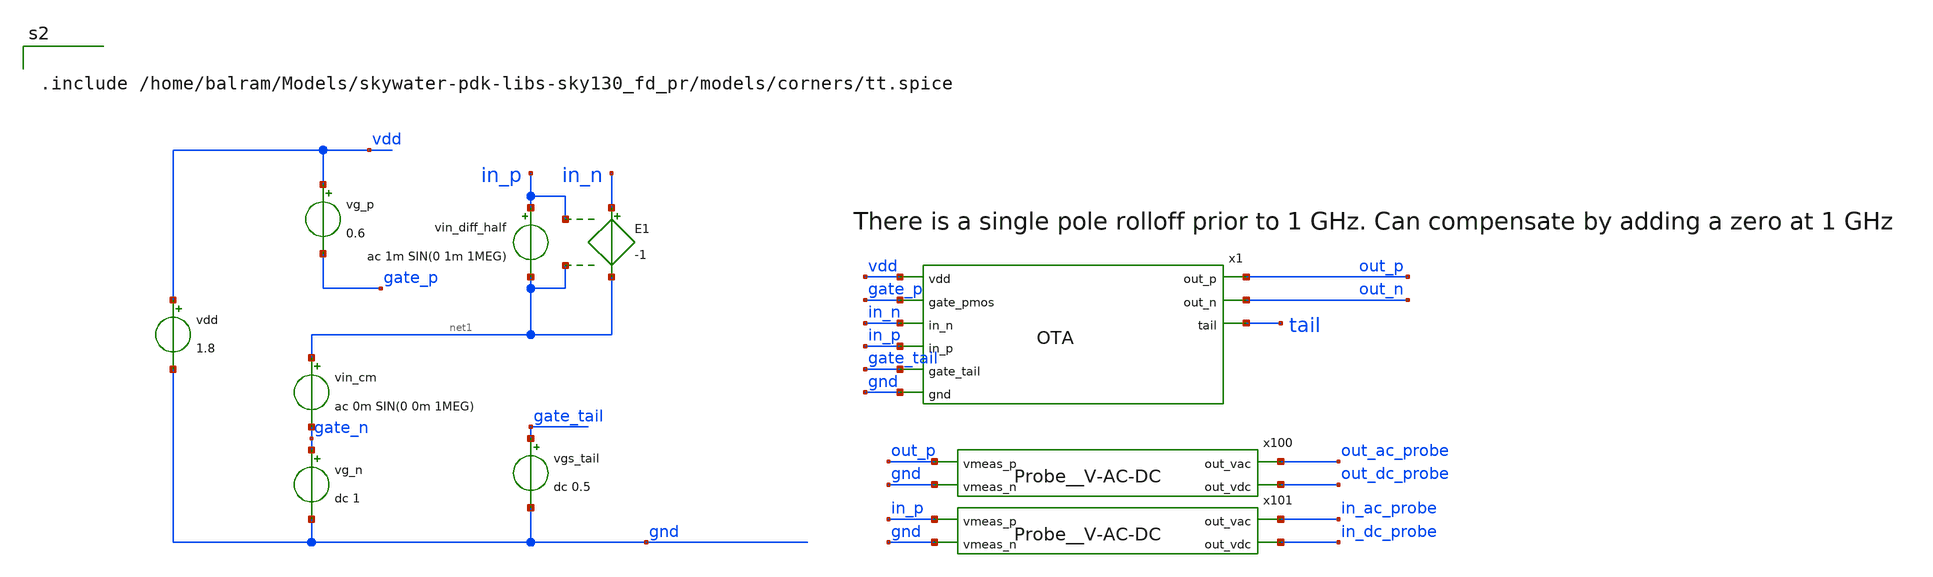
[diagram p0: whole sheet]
** sch_path: Amplifiers/OTA/TB__OTA.sch
**.subckt TB__OTA
vdd vdd gnd 1.8
vg_n gate_n gnd dc 1
vg_p vdd gate_p 0.6
x100 out_ac_probe out_p gnd out_dc_probe Probe__V-AC-DC
x101 in_ac_probe in_p gnd in_dc_probe Probe__V-AC-DC
x1 vdd gate_p out_p out_n in_n in_p tail gate_tail gnd OTA
vin_diff_half in_p net1 ac 1m SIN(0 1m 1MEG)
vin_cm net1 gate_n ac 0m SIN(0 0m 1MEG)
vgs_tail gate_tail gnd dc 0.5
E1 in_n net1 in_p net1 -1
**** begin user architecture code


.include /home/balram/Models/skywater-pdk-libs-sky130_fd_pr/models/corners/tt.spice


**** end user architecture code
**.ends

* expanding   symbol:
*+  /home/balram/Models/Circuit-Design/SKY130-Basic-RF-Blocks/Utilities/ProbeBlock/Probe__V-AC-DC.sym # of pins=4
** sym_path: Utilities/ProbeBlock/Probe__V-AC-DC.sym
** sch_path: Utilities/ProbeBlock/Probe__V-AC-DC.sch
.subckt Probe__V-AC-DC out_vac vmeas_p vmeas_n out_vdc
*.ipin vmeas_p
*.opin out_vac
*.opin out_vdc
*.ipin vmeas_n
E1 vcopy_p vmeas_n vmeas_p vmeas_n 1
C1 out_vac vcopy_p 1m m=1
R1 out_vac vmeas_n 1MEG m=1
C2 vmeas_n out_vdc 1m m=1
R2 out_vdc vcopy_p 1 m=1
.ends


* expanding   symbol:  OTA.sym # of pins=9
** sym_path: Amplifiers/OTA/OTA.sym
** sch_path: Amplifiers/OTA/OTA.sch
.subckt OTA vdd gate_pmos out_p out_n in_n in_p tail gate_tail gnd
*.ipin gate_pmos
*.ipin vdd
*.ipin in_p
*.ipin in_n
*.ipin gnd
*.opin out_p
*.opin out_n
*.ipin gate_tail
*.opin tail
XM1 out_p in_p tail gnd sky130_fd_pr__nfet_01v8_lvt L=1 W=100 nf=1 ad='int((nf+1)/2) * W/nf * 0.29' as='int((nf+2)/2) * W/nf * 0.29'
+ pd='2*int((nf+1)/2) * (W/nf + 0.29)' ps='2*int((nf+2)/2) * (W/nf + 0.29)' nrd='0.29 / W' nrs='0.29 / W'
+ sa=0 sb=0 sd=0 mult=2 m=2
XM2 out_n in_n tail gnd sky130_fd_pr__nfet_01v8_lvt L=1 W=100 nf=1 ad='int((nf+1)/2) * W/nf * 0.29' as='int((nf+2)/2) * W/nf * 0.29'
+ pd='2*int((nf+1)/2) * (W/nf + 0.29)' ps='2*int((nf+2)/2) * (W/nf + 0.29)' nrd='0.29 / W' nrs='0.29 / W'
+ sa=0 sb=0 sd=0 mult=2 m=2
XM10 out_p gate_pmos vdd vdd sky130_fd_pr__pfet_01v8_lvt L=1 W=90 nf=1 ad='int((1 + 1)/2) * 90 / 1 * 0.29'
+ as='int((1 + 2)/2) * 90 / 1 * 0.29' pd='2*int((1 + 1)/2) * (90 / 1 + 0.29)' ps='2*int((1 + 2)/2) * (90 / 1 + 0.29)'
+ nrd='0.29 / 90 ' nrs='0.29 / 90 ' sa=0 sb=0 sd=0 mult=2 m=2
XM11 out_n gate_pmos vdd vdd sky130_fd_pr__pfet_01v8_lvt L=1 W=90 nf=1 ad='int((1 + 1)/2) * 90 / 1 * 0.29'
+ as='int((1 + 2)/2) * 90 / 1 * 0.29' pd='2*int((1 + 1)/2) * (90 / 1 + 0.29)' ps='2*int((1 + 2)/2) * (90 / 1 + 0.29)'
+ nrd='0.29 / 90 ' nrs='0.29 / 90 ' sa=0 sb=0 sd=0 mult=2 m=2
XM3 tail gate_tail gnd gnd sky130_fd_pr__nfet_01v8_lvt L=10 W=100 nf=1 ad='int((nf+1)/2) * W/nf * 0.29'
+ as='int((nf+2)/2) * W/nf * 0.29' pd='2*int((nf+1)/2) * (W/nf + 0.29)' ps='2*int((nf+2)/2) * (W/nf + 0.29)'
+ nrd='0.29 / W' nrs='0.29 / W' sa=0 sb=0 sd=0 mult=20 m=20
.ends

.end
